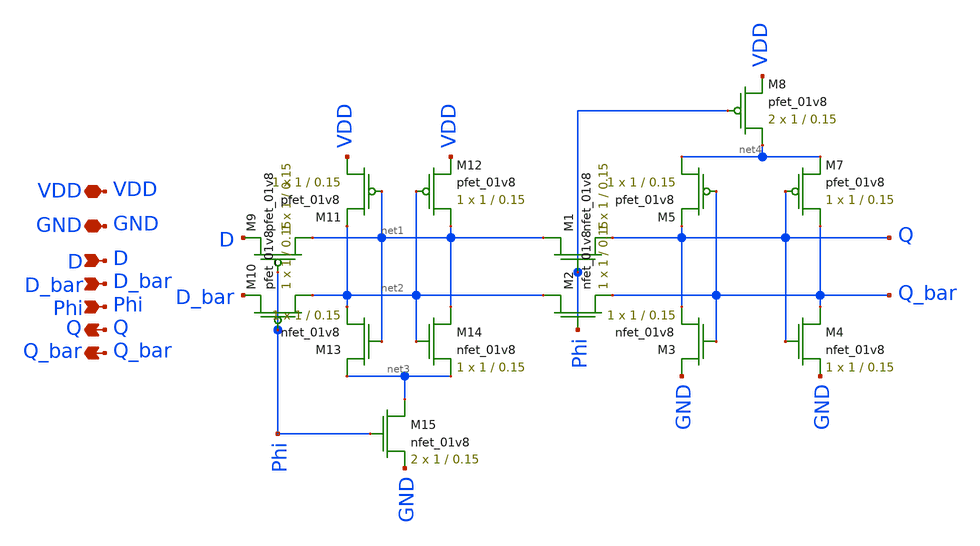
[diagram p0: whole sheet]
** sch_path: Homework2/Dlatch_xschem.sch
**.subckt Dlatch_xschem VDD GND D D_bar Phi Q Q_bar
*.iopin VDD
*.iopin GND
*.ipin D
*.ipin D_bar
*.ipin Phi
*.opin Q
*.opin Q_bar
XM1 net1 Phi Q GND sky130_fd_pr__nfet_01v8 L=0.15 W=1 nf=1 ad='int((nf+1)/2) * W/nf * 0.29' as='int((nf+2)/2) * W/nf * 0.29'
+ pd='2*int((nf+1)/2) * (W/nf + 0.29)' ps='2*int((nf+2)/2) * (W/nf + 0.29)' nrd='0.29 / W' nrs='0.29 / W'
+ sa=0 sb=0 sd=0 mult=1 m=1
XM2 net2 Phi Q_bar GND sky130_fd_pr__nfet_01v8 L=0.15 W=1 nf=1 ad='int((nf+1)/2) * W/nf * 0.29' as='int((nf+2)/2) * W/nf * 0.29'
+ pd='2*int((nf+1)/2) * (W/nf + 0.29)' ps='2*int((nf+2)/2) * (W/nf + 0.29)' nrd='0.29 / W' nrs='0.29 / W'
+ sa=0 sb=0 sd=0 mult=1 m=1
XM3 GND Q_bar Q GND sky130_fd_pr__nfet_01v8 L=0.15 W=1 nf=1 ad='int((nf+1)/2) * W/nf * 0.29' as='int((nf+2)/2) * W/nf * 0.29'
+ pd='2*int((nf+1)/2) * (W/nf + 0.29)' ps='2*int((nf+2)/2) * (W/nf + 0.29)' nrd='0.29 / W' nrs='0.29 / W'
+ sa=0 sb=0 sd=0 mult=1 m=1
XM4 Q_bar Q GND GND sky130_fd_pr__nfet_01v8 L=0.15 W=1 nf=1 ad='int((nf+1)/2) * W/nf * 0.29' as='int((nf+2)/2) * W/nf * 0.29'
+ pd='2*int((nf+1)/2) * (W/nf + 0.29)' ps='2*int((nf+2)/2) * (W/nf + 0.29)' nrd='0.29 / W' nrs='0.29 / W'
+ sa=0 sb=0 sd=0 mult=1 m=1
XM5 net4 Q_bar Q VDD sky130_fd_pr__pfet_01v8 L=0.15 W=1 nf=1 ad='int((nf+1)/2) * W/nf * 0.29' as='int((nf+2)/2) * W/nf * 0.29'
+ pd='2*int((nf+1)/2) * (W/nf + 0.29)' ps='2*int((nf+2)/2) * (W/nf + 0.29)' nrd='0.29 / W' nrs='0.29 / W'
+ sa=0 sb=0 sd=0 mult=1 m=1
XM7 Q_bar Q net4 VDD sky130_fd_pr__pfet_01v8 L=0.15 W=1 nf=1 ad='int((nf+1)/2) * W/nf * 0.29' as='int((nf+2)/2) * W/nf * 0.29'
+ pd='2*int((nf+1)/2) * (W/nf + 0.29)' ps='2*int((nf+2)/2) * (W/nf + 0.29)' nrd='0.29 / W' nrs='0.29 / W'
+ sa=0 sb=0 sd=0 mult=1 m=1
XM8 net4 Phi VDD VDD sky130_fd_pr__pfet_01v8 L=0.15 W=1 nf=1 ad='int((nf+1)/2) * W/nf * 0.29' as='int((nf+2)/2) * W/nf * 0.29'
+ pd='2*int((nf+1)/2) * (W/nf + 0.29)' ps='2*int((nf+2)/2) * (W/nf + 0.29)' nrd='0.29 / W' nrs='0.29 / W'
+ sa=0 sb=0 sd=0 mult=2 m=2
XM9 net1 Phi D VDD sky130_fd_pr__pfet_01v8 L=0.15 W=1 nf=1 ad='int((nf+1)/2) * W/nf * 0.29' as='int((nf+2)/2) * W/nf * 0.29'
+ pd='2*int((nf+1)/2) * (W/nf + 0.29)' ps='2*int((nf+2)/2) * (W/nf + 0.29)' nrd='0.29 / W' nrs='0.29 / W'
+ sa=0 sb=0 sd=0 mult=1 m=1
XM10 net2 Phi D_bar VDD sky130_fd_pr__pfet_01v8 L=0.15 W=1 nf=1 ad='int((nf+1)/2) * W/nf * 0.29' as='int((nf+2)/2) * W/nf * 0.29'
+ pd='2*int((nf+1)/2) * (W/nf + 0.29)' ps='2*int((nf+2)/2) * (W/nf + 0.29)' nrd='0.29 / W' nrs='0.29 / W'
+ sa=0 sb=0 sd=0 mult=1 m=1
XM11 VDD net1 net2 VDD sky130_fd_pr__pfet_01v8 L=0.15 W=1 nf=1 ad='int((nf+1)/2) * W/nf * 0.29' as='int((nf+2)/2) * W/nf * 0.29'
+ pd='2*int((nf+1)/2) * (W/nf + 0.29)' ps='2*int((nf+2)/2) * (W/nf + 0.29)' nrd='0.29 / W' nrs='0.29 / W'
+ sa=0 sb=0 sd=0 mult=1 m=1
XM12 net1 net2 VDD VDD sky130_fd_pr__pfet_01v8 L=0.15 W=1 nf=1 ad='int((nf+1)/2) * W/nf * 0.29' as='int((nf+2)/2) * W/nf * 0.29'
+ pd='2*int((nf+1)/2) * (W/nf + 0.29)' ps='2*int((nf+2)/2) * (W/nf + 0.29)' nrd='0.29 / W' nrs='0.29 / W'
+ sa=0 sb=0 sd=0 mult=1 m=1
XM13 net3 net1 net2 GND sky130_fd_pr__nfet_01v8 L=0.15 W=1 nf=1 ad='int((nf+1)/2) * W/nf * 0.29' as='int((nf+2)/2) * W/nf * 0.29'
+ pd='2*int((nf+1)/2) * (W/nf + 0.29)' ps='2*int((nf+2)/2) * (W/nf + 0.29)' nrd='0.29 / W' nrs='0.29 / W'
+ sa=0 sb=0 sd=0 mult=1 m=1
XM14 net1 net2 net3 GND sky130_fd_pr__nfet_01v8 L=0.15 W=1 nf=1 ad='int((nf+1)/2) * W/nf * 0.29' as='int((nf+2)/2) * W/nf * 0.29'
+ pd='2*int((nf+1)/2) * (W/nf + 0.29)' ps='2*int((nf+2)/2) * (W/nf + 0.29)' nrd='0.29 / W' nrs='0.29 / W'
+ sa=0 sb=0 sd=0 mult=1 m=1
XM15 net3 Phi GND GND sky130_fd_pr__nfet_01v8 L=0.15 W=1 nf=1 ad='int((nf+1)/2) * W/nf * 0.29' as='int((nf+2)/2) * W/nf * 0.29'
+ pd='2*int((nf+1)/2) * (W/nf + 0.29)' ps='2*int((nf+2)/2) * (W/nf + 0.29)' nrd='0.29 / W' nrs='0.29 / W'
+ sa=0 sb=0 sd=0 mult=2 m=2
**.ends
.end
